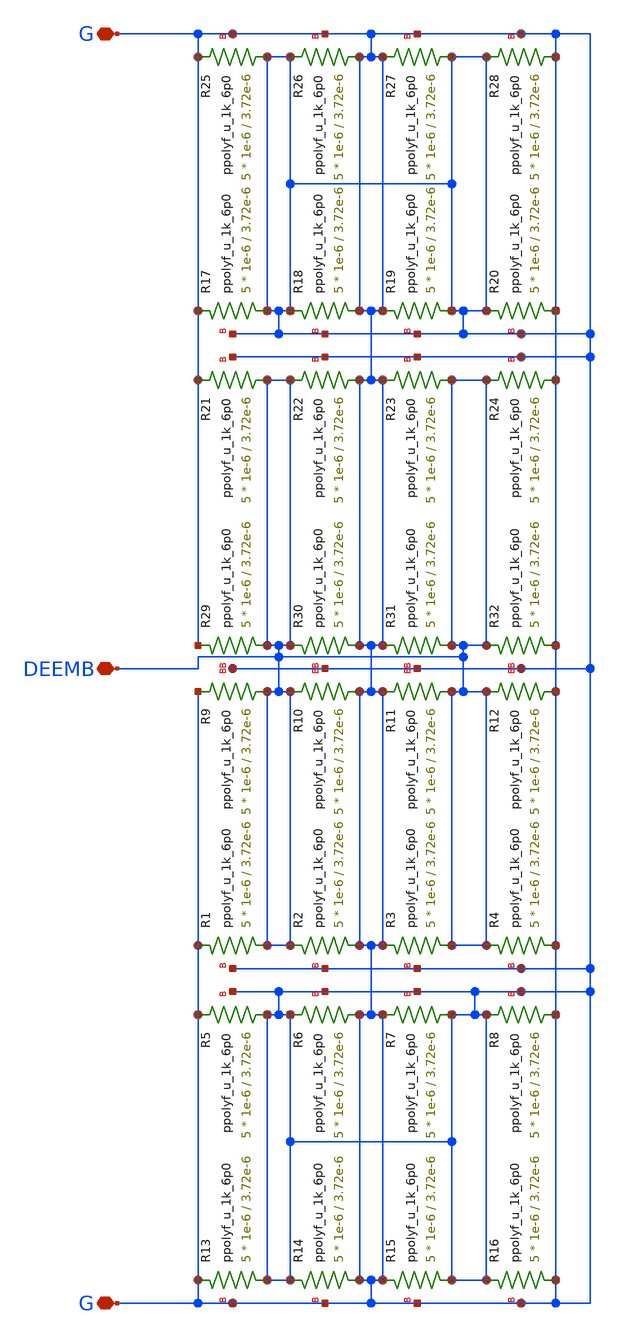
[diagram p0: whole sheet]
** sch_path: xschem/DEEMB_R.sch
**.subckt DEEMB_R G DEEMB G
*.iopin G
*.iopin DEEMB
*.iopin G
XR1 DEEMB G G ppolyf_u_1k_6p0 r_width=1e-6 r_length=3.72e-6 m=5
XR2 G DEEMB G ppolyf_u_1k_6p0 r_width=1e-6 r_length=3.72e-6 m=5
XR3 DEEMB G G ppolyf_u_1k_6p0 r_width=1e-6 r_length=3.72e-6 m=5
XR4 G DEEMB G ppolyf_u_1k_6p0 r_width=1e-6 r_length=3.72e-6 m=5
XR5 G G G ppolyf_u_1k_6p0 r_width=1e-6 r_length=3.72e-6 m=5
XR6 G G G ppolyf_u_1k_6p0 r_width=1e-6 r_length=3.72e-6 m=5
XR7 G G G ppolyf_u_1k_6p0 r_width=1e-6 r_length=3.72e-6 m=5
XR8 G G G ppolyf_u_1k_6p0 r_width=1e-6 r_length=3.72e-6 m=5
XR9 DEEMB G G ppolyf_u_1k_6p0 r_width=1e-6 r_length=3.72e-6 m=5
XR10 G DEEMB G ppolyf_u_1k_6p0 r_width=1e-6 r_length=3.72e-6 m=5
XR11 DEEMB G G ppolyf_u_1k_6p0 r_width=1e-6 r_length=3.72e-6 m=5
XR12 G DEEMB G ppolyf_u_1k_6p0 r_width=1e-6 r_length=3.72e-6 m=5
XR13 G G G ppolyf_u_1k_6p0 r_width=1e-6 r_length=3.72e-6 m=5
XR14 G G G ppolyf_u_1k_6p0 r_width=1e-6 r_length=3.72e-6 m=5
XR15 G G G ppolyf_u_1k_6p0 r_width=1e-6 r_length=3.72e-6 m=5
XR16 G G G ppolyf_u_1k_6p0 r_width=1e-6 r_length=3.72e-6 m=5
XR17 G G G ppolyf_u_1k_6p0 r_width=1e-6 r_length=3.72e-6 m=5
XR18 G G G ppolyf_u_1k_6p0 r_width=1e-6 r_length=3.72e-6 m=5
XR19 G G G ppolyf_u_1k_6p0 r_width=1e-6 r_length=3.72e-6 m=5
XR20 G G G ppolyf_u_1k_6p0 r_width=1e-6 r_length=3.72e-6 m=5
XR21 DEEMB G G ppolyf_u_1k_6p0 r_width=1e-6 r_length=3.72e-6 m=5
XR22 G DEEMB G ppolyf_u_1k_6p0 r_width=1e-6 r_length=3.72e-6 m=5
XR23 DEEMB G G ppolyf_u_1k_6p0 r_width=1e-6 r_length=3.72e-6 m=5
XR24 G DEEMB G ppolyf_u_1k_6p0 r_width=1e-6 r_length=3.72e-6 m=5
XR25 G G G ppolyf_u_1k_6p0 r_width=1e-6 r_length=3.72e-6 m=5
XR26 G G G ppolyf_u_1k_6p0 r_width=1e-6 r_length=3.72e-6 m=5
XR27 G G G ppolyf_u_1k_6p0 r_width=1e-6 r_length=3.72e-6 m=5
XR28 G G G ppolyf_u_1k_6p0 r_width=1e-6 r_length=3.72e-6 m=5
XR29 DEEMB G G ppolyf_u_1k_6p0 r_width=1e-6 r_length=3.72e-6 m=5
XR30 G DEEMB G ppolyf_u_1k_6p0 r_width=1e-6 r_length=3.72e-6 m=5
XR31 DEEMB G G ppolyf_u_1k_6p0 r_width=1e-6 r_length=3.72e-6 m=5
XR32 G DEEMB G ppolyf_u_1k_6p0 r_width=1e-6 r_length=3.72e-6 m=5
**.ends
.end
